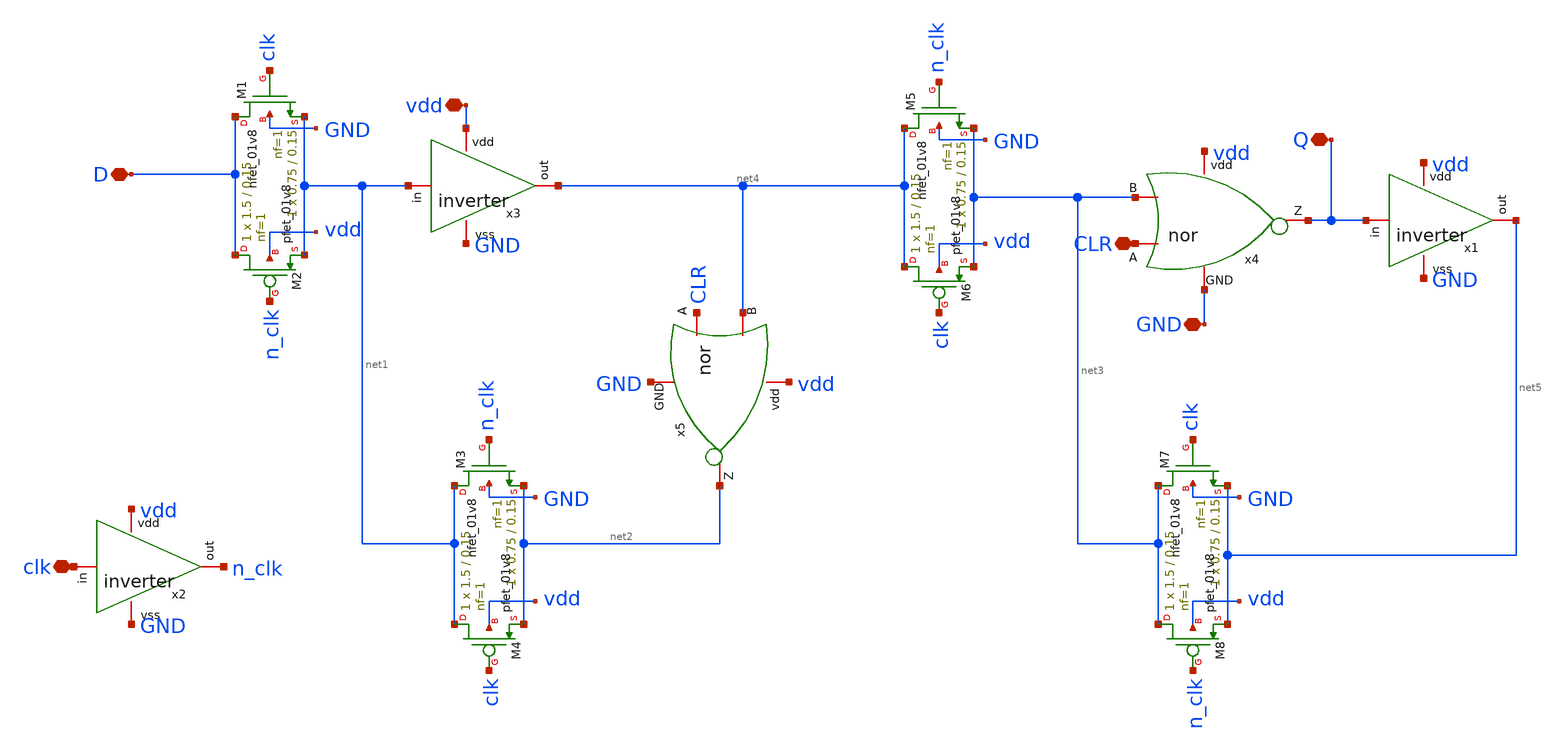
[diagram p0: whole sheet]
** sch_path: simbolos y esquematicos/FFD.sch
**.subckt FFD D clk vdd GND CLR Q
*.iopin D
*.iopin clk
*.iopin vdd
*.iopin GND
*.iopin CLR
*.iopin Q
x1 vdd Q net5 GND inverter
x2 vdd clk n_clk GND inverter
x3 vdd net1 net4 GND inverter
x4 vdd Q net3 CLR GND nor
x5 vdd net2 net4 CLR GND nor
XM1 D clk net1 GND sky130_fd_pr__nfet_01v8 L=0.15 W=0.75 nf=1 ad='int((nf+1)/2) * W/nf * 0.29' as='int((nf+2)/2) * W/nf * 0.29'
+ pd='2*int((nf+1)/2) * (W/nf + 0.29)' ps='2*int((nf+2)/2) * (W/nf + 0.29)' nrd='0.29 / W' nrs='0.29 / W'
+ sa=0 sb=0 sd=0 mult=1 m=1
XM2 D n_clk net1 vdd sky130_fd_pr__pfet_01v8 L=0.15 W=1.5 nf=1 ad='int((nf+1)/2) * W/nf * 0.29' as='int((nf+2)/2) * W/nf * 0.29'
+ pd='2*int((nf+1)/2) * (W/nf + 0.29)' ps='2*int((nf+2)/2) * (W/nf + 0.29)' nrd='0.29 / W' nrs='0.29 / W'
+ sa=0 sb=0 sd=0 mult=1 m=1
XM3 net1 n_clk net2 GND sky130_fd_pr__nfet_01v8 L=0.15 W=0.75 nf=1 ad='int((nf+1)/2) * W/nf * 0.29' as='int((nf+2)/2) * W/nf * 0.29'
+ pd='2*int((nf+1)/2) * (W/nf + 0.29)' ps='2*int((nf+2)/2) * (W/nf + 0.29)' nrd='0.29 / W' nrs='0.29 / W'
+ sa=0 sb=0 sd=0 mult=1 m=1
XM4 net1 clk net2 vdd sky130_fd_pr__pfet_01v8 L=0.15 W=1.5 nf=1 ad='int((nf+1)/2) * W/nf * 0.29' as='int((nf+2)/2) * W/nf * 0.29'
+ pd='2*int((nf+1)/2) * (W/nf + 0.29)' ps='2*int((nf+2)/2) * (W/nf + 0.29)' nrd='0.29 / W' nrs='0.29 / W'
+ sa=0 sb=0 sd=0 mult=1 m=1
XM5 net4 n_clk net3 GND sky130_fd_pr__nfet_01v8 L=0.15 W=0.75 nf=1 ad='int((nf+1)/2) * W/nf * 0.29' as='int((nf+2)/2) * W/nf * 0.29'
+ pd='2*int((nf+1)/2) * (W/nf + 0.29)' ps='2*int((nf+2)/2) * (W/nf + 0.29)' nrd='0.29 / W' nrs='0.29 / W'
+ sa=0 sb=0 sd=0 mult=1 m=1
XM6 net4 clk net3 vdd sky130_fd_pr__pfet_01v8 L=0.15 W=1.5 nf=1 ad='int((nf+1)/2) * W/nf * 0.29' as='int((nf+2)/2) * W/nf * 0.29'
+ pd='2*int((nf+1)/2) * (W/nf + 0.29)' ps='2*int((nf+2)/2) * (W/nf + 0.29)' nrd='0.29 / W' nrs='0.29 / W'
+ sa=0 sb=0 sd=0 mult=1 m=1
XM7 net3 clk net5 GND sky130_fd_pr__nfet_01v8 L=0.15 W=0.75 nf=1 ad='int((nf+1)/2) * W/nf * 0.29' as='int((nf+2)/2) * W/nf * 0.29'
+ pd='2*int((nf+1)/2) * (W/nf + 0.29)' ps='2*int((nf+2)/2) * (W/nf + 0.29)' nrd='0.29 / W' nrs='0.29 / W'
+ sa=0 sb=0 sd=0 mult=1 m=1
XM8 net3 n_clk net5 vdd sky130_fd_pr__pfet_01v8 L=0.15 W=1.5 nf=1 ad='int((nf+1)/2) * W/nf * 0.29' as='int((nf+2)/2) * W/nf * 0.29'
+ pd='2*int((nf+1)/2) * (W/nf + 0.29)' ps='2*int((nf+2)/2) * (W/nf + 0.29)' nrd='0.29 / W' nrs='0.29 / W'
+ sa=0 sb=0 sd=0 mult=1 m=1
**.ends
.end
